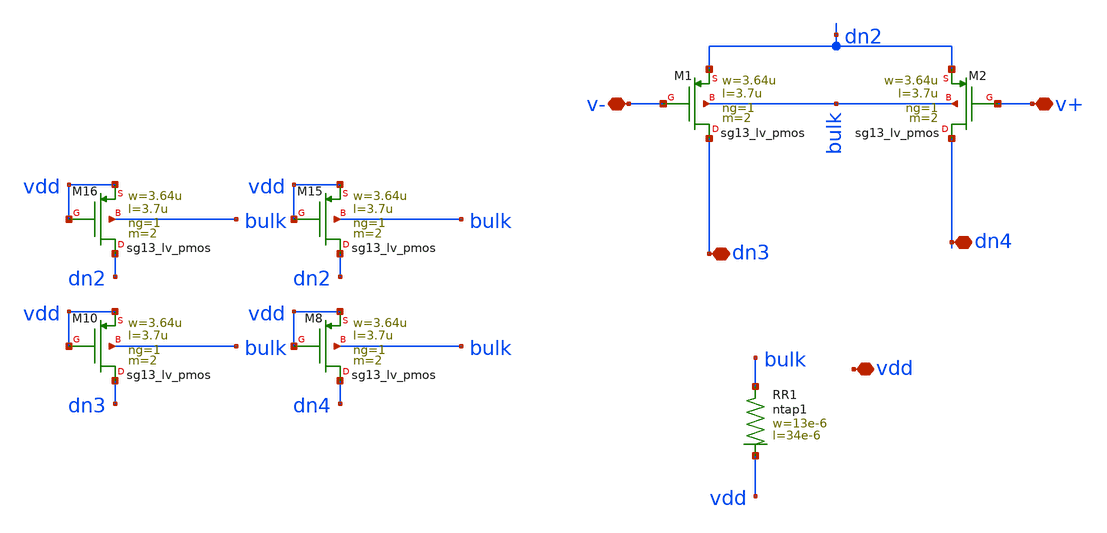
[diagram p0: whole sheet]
** sch_path: modules/module_1_bandgap_reference/part_3_layout/OTA_layout/input_pair/schematic_mod/input_common_centroid.sch
**.subckt input_common_centroid v- v+ vdd dn3 dn4
*.iopin v-
*.iopin v+
*.iopin vdd
*.iopin dn3
*.iopin dn4
XM1 dn3 v- dn2 bulk sg13_lv_pmos w=3.64u l=3.7u ng=1 m=2 mm_ok=1
XM2 dn4 v+ dn2 bulk sg13_lv_pmos w=3.64u l=3.7u ng=1 m=2 mm_ok=1
XM8 dn4 vdd vdd bulk sg13_lv_pmos w=3.64u l=3.7u ng=1 m=2 mm_ok=1
XM10 dn3 vdd vdd bulk sg13_lv_pmos w=3.64u l=3.7u ng=1 m=2 mm_ok=1
XM15 dn2 vdd vdd bulk sg13_lv_pmos w=3.64u l=3.7u ng=1 m=2 mm_ok=1
XM16 dn2 vdd vdd bulk sg13_lv_pmos w=3.64u l=3.7u ng=1 m=2 mm_ok=1
XR1 bulk vdd ntap1 R=1.828 w=13e-6 l=34e-6
**.ends
.end
